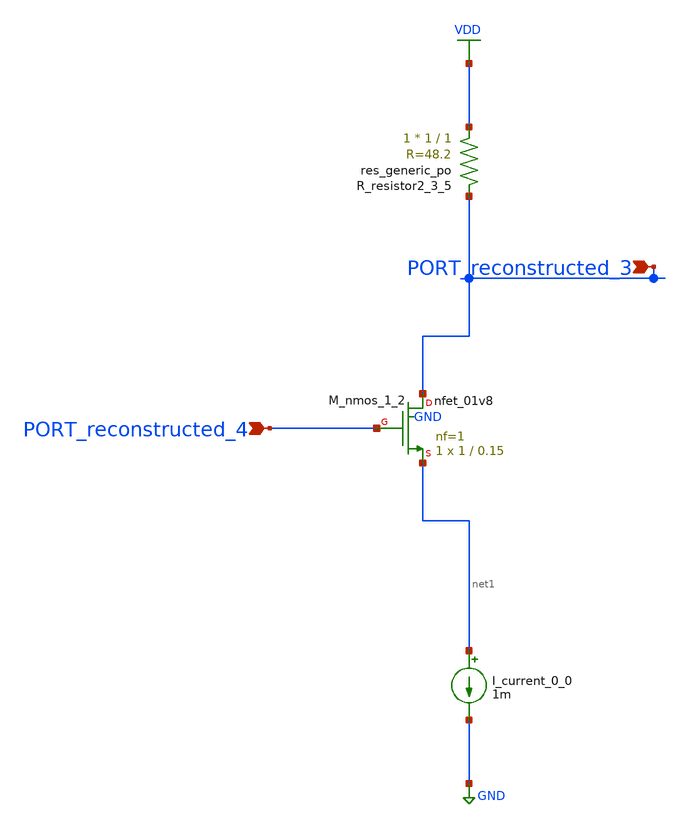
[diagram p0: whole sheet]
** sch_path: schematics/AMSNet/129.sch
**.subckt 129 PORT_reconstructed_4 PORT_reconstructed_3
*.ipin PORT_reconstructed_4
*.ipin PORT_reconstructed_3
I_current_0_0 net1 GND 1m
XM_nmos_1_2 PORT_reconstructed_3 PORT_reconstructed_4 net1 GND sky130_fd_pr__nfet_01v8 L=0.15 W=1 nf=1
+ ad='int((1 + 1)/2) * 1 / 1 * 0.29' as='int((1 + 2)/2) * 1 / 1 * 0.29' pd='2*int((1 + 1)/2) * (1 / 1 + 0.29)'
+ ps='2*int((1 + 2)/2) * (1 / 1 + 0.29)' nrd='0.29 / 1 ' nrs='0.29 / 1 ' sa=0 sb=0 sd=0 mult=1 m=1
XR_resistor2_3_5 VDD PORT_reconstructed_3 sky130_fd_pr__res_generic_po W=1 L=1 m=1
**.ends
.GLOBAL GND
.GLOBAL VDD
.end
